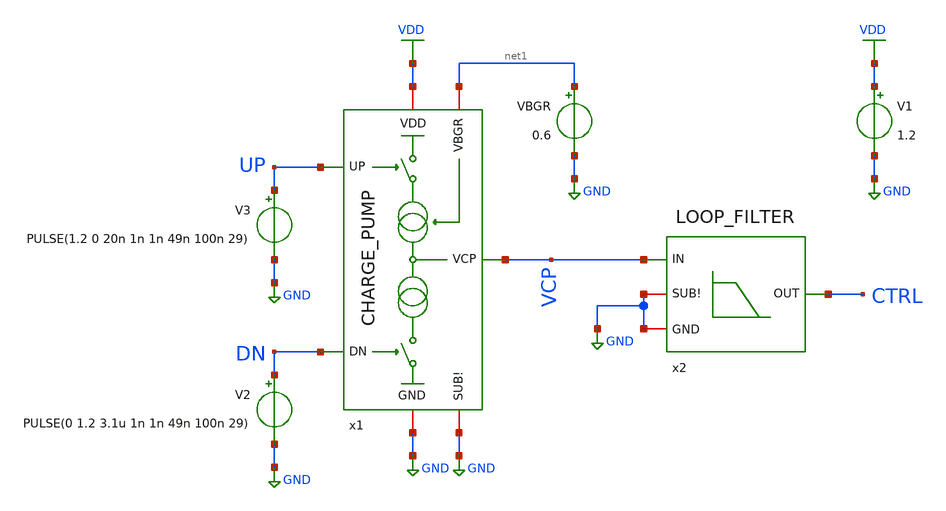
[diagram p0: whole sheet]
** sch_path: xschem/charge-pump/tb_CP_LF.sch
**.subckt tb_CP_LF
V1 VDD GND 1.2
V2 DN GND PULSE(0 1.2 3.1u 1n 1n 49n 100n 29)
V3 UP GND PULSE(1.2 0 20n 1n 1n 49n 100n 29)
VBGR net1 GND 0.6
x1 UP VDD VCP net1 GND DN GND CHARGE_PUMP
x2 CTRL VCP GND GND LOOP_FILTER
**** begin user architecture code



.include tb_CP.save
.param temp=27
.option method=gear rshunt=1.0e12
.control
save all
op
write tb_CP_LF.raw
.endc




.lib cornerMOSlv.lib mos_tt
.lib cornerMOShv.lib mos_tt
.lib cornerRES.lib res_typ
.lib cornerCAP.lib cap_typ




.param temp = 27
.options method=gear rshunt=1.0e12

.control

* Save required signals
save v(UP) v(DN) v(VCP) v(CTRL)

* Long transient simulation
tran 1n 6u

* Plot transient waveform
plot v(UP) v(DN) v(VCP) v(CTRL)
plot v(CTRL)

.endc



**** end user architecture code
**.ends
.GLOBAL VDD
.GLOBAL GND
.end
